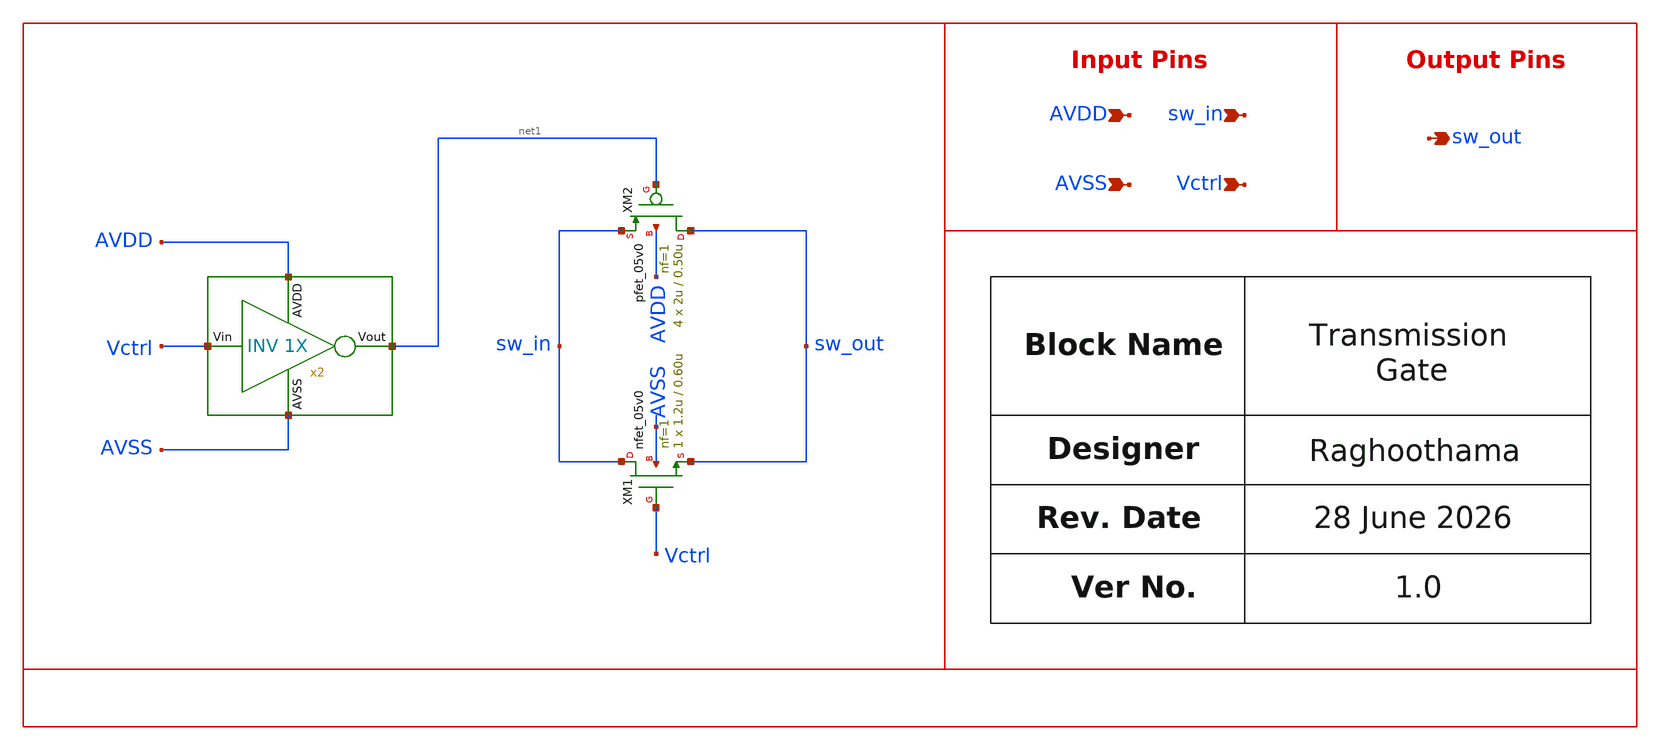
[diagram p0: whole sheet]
** sch_path: design/schematics/ADC_Buffer/rrao_cic_bms_afe_iadc_tg_switch.sch
**.subckt rrao_cic_bms_afe_iadc_tg_switch sw_in sw_out Vctrl AVDD AVSS
*.ipin sw_in
*.opin sw_out
*.ipin Vctrl
*.ipin AVDD
*.ipin AVSS
XM1 sw_in Vctrl sw_out AVSS nfet_05v0 L=0.60u W=1.2u nf=1 ad='int((nf+1)/2) * W/nf * 0.18u' as='int((nf+2)/2) * W/nf * 0.18u'
+ pd='2*int((nf+1)/2) * (W/nf + 0.18u)' ps='2*int((nf+2)/2) * (W/nf + 0.18u)' nrd='0.18u / W' nrs='0.18u / W'
+ sa=0 sb=0 sd=0 m=1
XM2 sw_out net1 sw_in AVDD pfet_05v0 L=0.50u W=2u nf=1 ad='int((nf+1)/2) * W/nf * 0.18u' as='int((nf+2)/2) * W/nf * 0.18u'
+ pd='2*int((nf+1)/2) * (W/nf + 0.18u)' ps='2*int((nf+2)/2) * (W/nf + 0.18u)' nrd='0.18u / W' nrs='0.18u / W'
+ sa=0 sb=0 sd=0 m=4
x2 AVDD net1 Vctrl AVSS sa_cic_bms_afe_iadc_quantizer_inv1x
**.ends
.end
